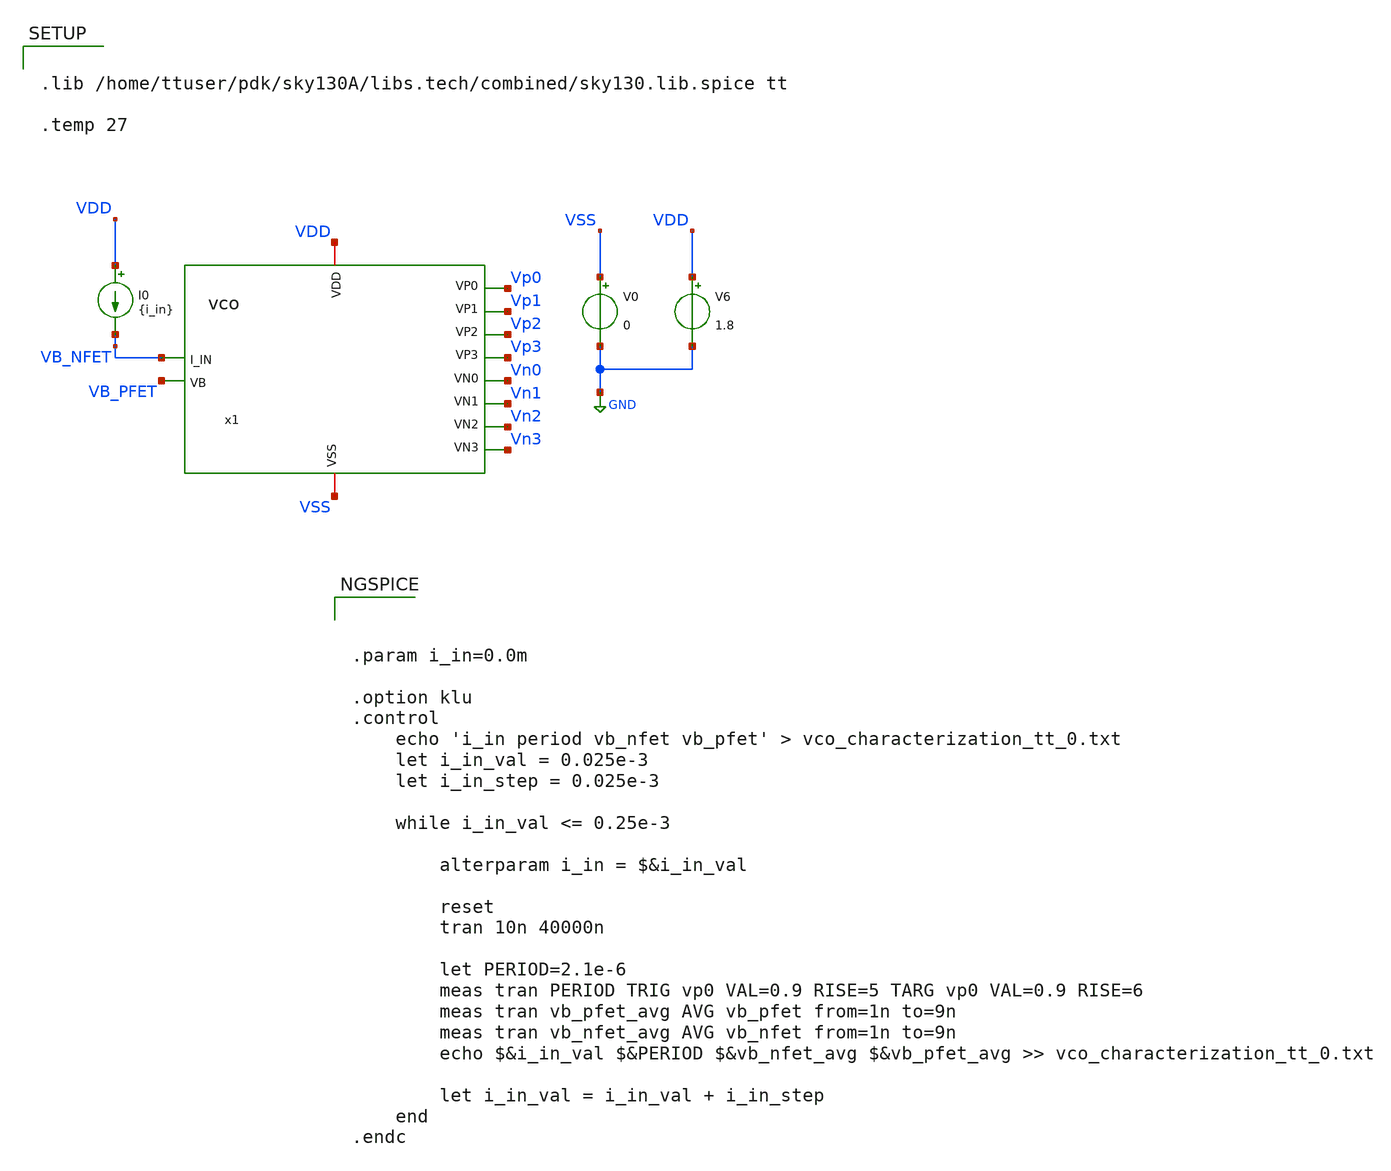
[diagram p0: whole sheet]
** sch_path: xschem/vco_characterization_tb.sch
**.subckt vco_characterization_tb
V0 VSS GND 0
V6 VDD GND 1.8
I0 VDD VB_NFET {i_in}
x1 VDD VSS VB_NFET Vp0 Vp1 Vp2 Vp3 Vn0 Vn1 Vn2 Vn3 VB_PFET vco
**** begin user architecture code



.param i_in=0.0m

.option klu
.control
	echo 'i_in period vb_nfet vb_pfet' > vco_characterization_tt_0.txt
	let i_in_val = 0.025e-3
	let i_in_step = 0.025e-3

	while i_in_val <= 0.25e-3

		alterparam i_in = $&i_in_val

		reset
		tran 10n 40000n

		let PERIOD=2.1e-6
		meas tran PERIOD TRIG vp0 VAL=0.9 RISE=5 TARG vp0 VAL=0.9 RISE=6
		meas tran vb_pfet_avg AVG vb_pfet from=1n to=9n
		meas tran vb_nfet_avg AVG vb_nfet from=1n to=9n
		echo $&i_in_val $&PERIOD $&vb_nfet_avg $&vb_pfet_avg >> vco_characterization_tt_0.txt

		let i_in_val = i_in_val + i_in_step
	end
.endc




.lib /home/ttuser/pdk/sky130A/libs.tech/combined/sky130.lib.spice tt

.temp 27


**** end user architecture code
**.ends
.GLOBAL GND
.end
